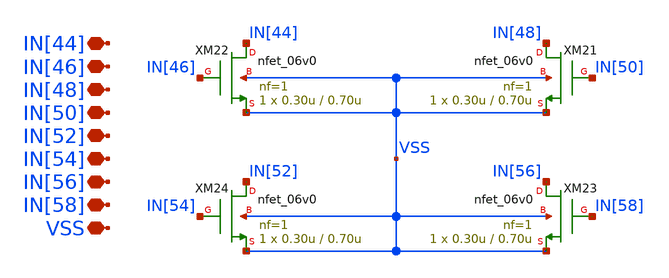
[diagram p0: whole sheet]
** sch_path: designs/libs/core_single-fet/nfet-com/nfet-com.sch
**.subckt nfet-com VSS IN[44] IN[46] IN[48] IN[50] IN[52] IN[54] IN[56] IN[58]
*.iopin VSS
*.iopin IN[44]
*.iopin IN[46]
*.iopin IN[48]
*.iopin IN[50]
*.iopin IN[52]
*.iopin IN[54]
*.iopin IN[56]
*.iopin IN[58]
XM21 IN[48] IN[50] VSS VSS nfet_06v0 L=0.70u W=0.30u nf=1 ad='int((nf+1)/2) * W/nf * 0.18u' as='int((nf+2)/2) * W/nf * 0.18u'
+ pd='2*int((nf+1)/2) * (W/nf + 0.18u)' ps='2*int((nf+2)/2) * (W/nf + 0.18u)' nrd='0.18u / W' nrs='0.18u / W'
+ sa=0 sb=0 sd=0 m=1
XM22 IN[44] IN[46] VSS VSS nfet_06v0 L=0.70u W=0.30u nf=1 ad='int((nf+1)/2) * W/nf * 0.18u' as='int((nf+2)/2) * W/nf * 0.18u'
+ pd='2*int((nf+1)/2) * (W/nf + 0.18u)' ps='2*int((nf+2)/2) * (W/nf + 0.18u)' nrd='0.18u / W' nrs='0.18u / W'
+ sa=0 sb=0 sd=0 m=1
XM23 IN[56] IN[58] VSS VSS nfet_06v0 L=0.70u W=0.30u nf=1 ad='int((nf+1)/2) * W/nf * 0.18u' as='int((nf+2)/2) * W/nf * 0.18u'
+ pd='2*int((nf+1)/2) * (W/nf + 0.18u)' ps='2*int((nf+2)/2) * (W/nf + 0.18u)' nrd='0.18u / W' nrs='0.18u / W'
+ sa=0 sb=0 sd=0 m=1
XM24 IN[52] IN[54] VSS VSS nfet_06v0 L=0.70u W=0.30u nf=1 ad='int((nf+1)/2) * W/nf * 0.18u' as='int((nf+2)/2) * W/nf * 0.18u'
+ pd='2*int((nf+1)/2) * (W/nf + 0.18u)' ps='2*int((nf+2)/2) * (W/nf + 0.18u)' nrd='0.18u / W' nrs='0.18u / W'
+ sa=0 sb=0 sd=0 m=1
**.ends
.end
